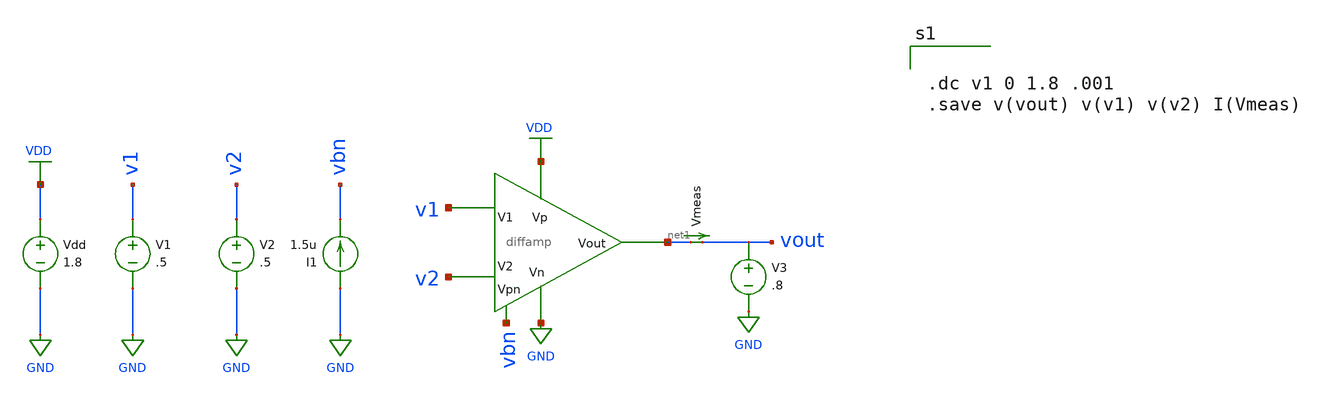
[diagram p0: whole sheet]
** sch_path: mini_proj_3/schematic/diff_2b.sch
**.subckt diff_2b
Vdd VDD GND 1.8
V1 v1 GND .5
V2 v2 GND .5
I1 GND vbn 1.5u
X1 vbn VDD GND v1 v2 net1 diffamp
V3 vout GND .8
Vmeas net1 vout 0
.save i(vmeas)
**** begin user architecture code

.option wnflag=1
.lib ~/skywater/skywater-pdk/libraries/sky130_fd_pr_ngspice/latest/models/sky130.lib.spice tt



.dc v1 0 1.8 .001
.save v(vout) v(v1) v(v2) I(Vmeas)


**** end user architecture code
**.ends
.GLOBAL VDD
.GLOBAL GND
.end
